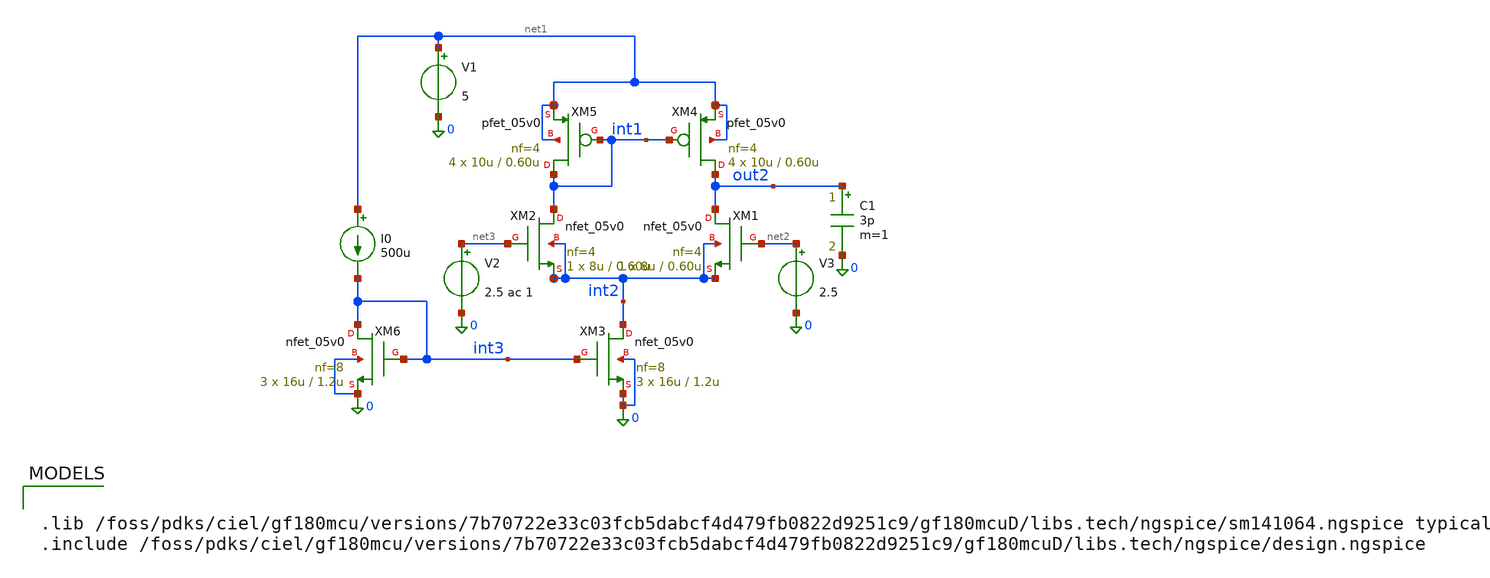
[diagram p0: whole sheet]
** sch_path: RN_Gm2/gm2_ota_tb.sch
**.subckt gm2_ota_tb
XM1 out2 net2 int2 int2 nfet_05v0 L=0.60u W=8u nf=4 ad='int((nf+1)/2) * W/nf * 0.18u' as='int((nf+2)/2) * W/nf * 0.18u'
+ pd='2*int((nf+1)/2) * (W/nf + 0.18u)' ps='2*int((nf+2)/2) * (W/nf + 0.18u)' nrd='0.18u / W' nrs='0.18u / W'
+ sa=0 sb=0 sd=0 m=1
XM2 int1 net3 int2 int2 nfet_05v0 L=0.60u W=8u nf=4 ad='int((nf+1)/2) * W/nf * 0.18u' as='int((nf+2)/2) * W/nf * 0.18u'
+ pd='2*int((nf+1)/2) * (W/nf + 0.18u)' ps='2*int((nf+2)/2) * (W/nf + 0.18u)' nrd='0.18u / W' nrs='0.18u / W'
+ sa=0 sb=0 sd=0 m=1
XM3 int2 int3 0 0 nfet_05v0 L=1.2u W=16u nf=8 ad='int((nf+1)/2) * W/nf * 0.18u' as='int((nf+2)/2) * W/nf * 0.18u'
+ pd='2*int((nf+1)/2) * (W/nf + 0.18u)' ps='2*int((nf+2)/2) * (W/nf + 0.18u)' nrd='0.18u / W' nrs='0.18u / W'
+ sa=0 sb=0 sd=0 m=3
XM4 out2 int1 net1 net1 pfet_05v0 L=0.60u W=10u nf=4 ad='int((nf+1)/2) * W/nf * 0.18u' as='int((nf+2)/2) * W/nf * 0.18u'
+ pd='2*int((nf+1)/2) * (W/nf + 0.18u)' ps='2*int((nf+2)/2) * (W/nf + 0.18u)' nrd='0.18u / W' nrs='0.18u / W'
+ sa=0 sb=0 sd=0 m=4
XM5 int1 int1 net1 net1 pfet_05v0 L=0.60u W=10u nf=4 ad='int((nf+1)/2) * W/nf * 0.18u' as='int((nf+2)/2) * W/nf * 0.18u'
+ pd='2*int((nf+1)/2) * (W/nf + 0.18u)' ps='2*int((nf+2)/2) * (W/nf + 0.18u)' nrd='0.18u / W' nrs='0.18u / W'
+ sa=0 sb=0 sd=0 m=4
V1 net1 0 5
V2 net3 0 2.5 ac 1
V3 net2 0 2.5
C1 out2 0 3p m=1
I0 net1 int3 500u
XM6 int3 int3 0 0 nfet_05v0 L=1.2u W=16u nf=8 ad='int((nf+1)/2) * W/nf * 0.18u' as='int((nf+2)/2) * W/nf * 0.18u'
+ pd='2*int((nf+1)/2) * (W/nf + 0.18u)' ps='2*int((nf+2)/2) * (W/nf + 0.18u)' nrd='0.18u / W' nrs='0.18u / W'
+ sa=0 sb=0 sd=0 m=3
**** begin user architecture code


.lib /foss/pdks/ciel/gf180mcu/versions/7b70722e33c03fcb5dabcf4d479fb0822d9251c9/gf180mcuD/libs.tech/ngspice/sm141064.ngspice typical
.include /foss/pdks/ciel/gf180mcu/versions/7b70722e33c03fcb5dabcf4d479fb0822d9251c9/gf180mcuD/libs.tech/ngspice/design.ngspice




.control
  	save all
	op
	ac dec 20 1 100Meg
	remzerovec
	write 1_OTA_ac.raw
.endc

.options savecurrents


**** end user architecture code
**.ends
.end
